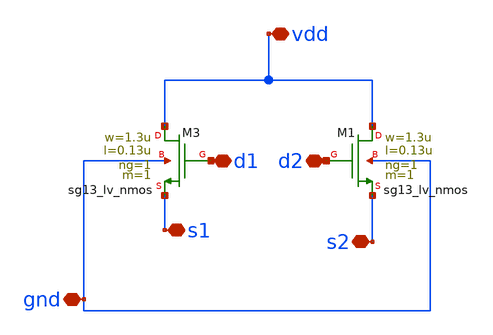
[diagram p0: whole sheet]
** sch_path: part_5_analog_layout/bootstrap/schematic/test_ng.sch
**.subckt test_ng s2 vdd gnd s1 d1 d2
*.iopin s2
*.iopin vdd
*.iopin gnd
*.iopin s1
*.iopin d1
*.iopin d2
XM3 vdd d1 s1 gnd sg13_lv_nmos w=1.3u l=0.13u ng=1 m=1 mm_ok=1
XM1 vdd d2 s2 gnd sg13_lv_nmos w=1.3u l=0.13u ng=1 m=1 mm_ok=1
**.ends
.end
